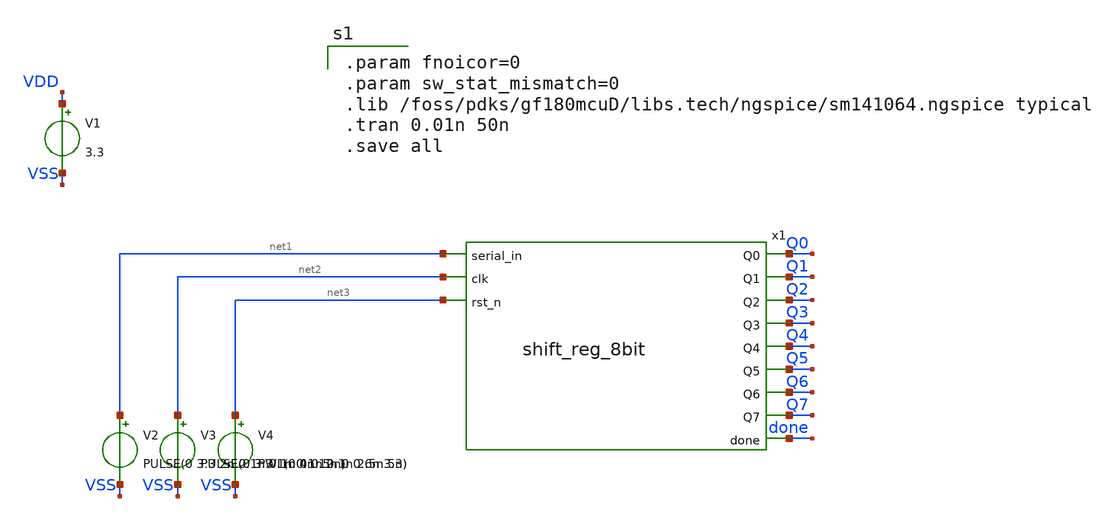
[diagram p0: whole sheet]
** sch_path: xschem/sar_adc/blocks/async_sar/testbench/tb_shift_reg_8bit.sch
**.subckt tb_shift_reg_8bit
V1 VDD VSS 3.3
V2 net1 VSS PULSE(0 3.3 2n 0.1n 0.1n 4n 12n)
V3 net2 VSS PULSE(0 3.3 1n 0.1n 0.1n 2.5n 5n)
V4 net3 VSS PWL(0 0 0.5n 0 0.6n 3.3)
x1 net1 net2 net3 Q0 Q1 Q2 Q3 Q4 Q5 Q6 Q7 done shift_reg_8bit
**** begin user architecture code

.param fnoicor=0
.param sw_stat_mismatch=0
.lib /foss/pdks/gf180mcuD/libs.tech/ngspice/sm141064.ngspice typical
.tran 0.01n 50n
.save all

**** end user architecture code
**.ends

* expanding   symbol:  sar_adc/blocks/async_sar/shift_reg_8bit.sym # of pins=12
** sym_path: xschem/sar_adc/blocks/async_sar/shift_reg_8bit.sym
** sch_path: xschem/sar_adc/blocks/async_sar/shift_reg_8bit.sch
.subckt shift_reg_8bit serial_in clk rst_n Q0 Q1 Q2 Q3 Q4 Q5 Q6 Q7 done
*.ipin serial_in
*.ipin clk
*.ipin rst_n
*.opin Q0
*.opin Q1
*.opin Q2
*.opin Q3
*.opin Q4
*.opin Q5
*.opin Q6
*.opin Q7
*.opin done
x1 Q0 clk rst_n serial_in clk rst_n dff_cell_set
x2 Q0 clk rst_n Q1 dff_cell
x3 Q1 clk rst_n Q2 dff_cell
x4 Q2 clk rst_n Q3 dff_cell
x5 Q3 clk rst_n Q4 dff_cell
x6 Q4 clk rst_n Q5 dff_cell
x7 Q5 clk rst_n Q6 dff_cell
x8 Q6 clk rst_n Q7 dff_cell
x9 Q7 clk rst_n done dff_cell
.ends


* expanding   symbol:  sar_adc/blocks/async_sar/dff_cell_set.sym # of pins=6
** sym_path: xschem/sar_adc/blocks/async_sar/dff_cell_set.sym
** sch_path: xschem/sar_adc/blocks/async_sar/dff_cell_set.sch
.subckt dff_cell_set vdd vss Q D clk rst_n
*.ipin D
*.ipin clk
*.ipin rst_n
*.opin Q
*.iopin vdd
*.iopin vss
x_inv_d vdd D D_b vdd async_inverter
x_dff D_b clk rst_n vdd dff_cell
x_inv_q vdd net1 Q vss async_inverter
.ends


* expanding   symbol:  sar_adc/blocks/async_sar/dff_cell.sym # of pins=4
** sym_path: xschem/sar_adc/dff_cell.sym
** sch_path: xschem/sar_adc/dff_cell.sch
.subckt dff_cell D clk rst_n Q
*.ipin clk
*.ipin D
*.ipin rst_n
*.opin Q
XM1 clk_n clk VDD VDD pfet_03v3 L=0.28u W=1.0u nf=1 ad='int((nf+1)/2) * W/nf * 0.18u' as='int((nf+2)/2) * W/nf * 0.18u'
+ pd='2*int((nf+1)/2) * (W/nf + 0.18u)' ps='2*int((nf+2)/2) * (W/nf + 0.18u)' nrd='0.18u / W' nrs='0.18u / W'
+ sa=0 sb=0 sd=0 m=1
XM2 clk_n clk 0 0 nfet_03v3 L=0.28u W=0.50u nf=1 ad='int((nf+1)/2) * W/nf * 0.18u' as='int((nf+2)/2) * W/nf * 0.18u'
+ pd='2*int((nf+1)/2) * (W/nf + 0.18u)' ps='2*int((nf+2)/2) * (W/nf + 0.18u)' nrd='0.18u / W' nrs='0.18u / W'
+ sa=0 sb=0 sd=0 m=1
XM3 M clk D_int VDD pfet_03v3 L=0.28u W=1.0u nf=1 ad='int((nf+1)/2) * W/nf * 0.18u' as='int((nf+2)/2) * W/nf * 0.18u'
+ pd='2*int((nf+1)/2) * (W/nf + 0.18u)' ps='2*int((nf+2)/2) * (W/nf + 0.18u)' nrd='0.18u / W' nrs='0.18u / W'
+ sa=0 sb=0 sd=0 m=1
XM4 D_int clk_n M 0 nfet_03v3 L=0.28u W=0.50u nf=1 ad='int((nf+1)/2) * W/nf * 0.18u' as='int((nf+2)/2) * W/nf * 0.18u'
+ pd='2*int((nf+1)/2) * (W/nf + 0.18u)' ps='2*int((nf+2)/2) * (W/nf + 0.18u)' nrd='0.18u / W' nrs='0.18u / W'
+ sa=0 sb=0 sd=0 m=1
XM5 M_bar M VDD VDD pfet_03v3 L=0.28u W=1.0u nf=1 ad='int((nf+1)/2) * W/nf * 0.18u' as='int((nf+2)/2) * W/nf * 0.18u'
+ pd='2*int((nf+1)/2) * (W/nf + 0.18u)' ps='2*int((nf+2)/2) * (W/nf + 0.18u)' nrd='0.18u / W' nrs='0.18u / W'
+ sa=0 sb=0 sd=0 m=1
XM6 M_bar M 0 0 nfet_03v3 L=0.28u W=0.50u nf=1 ad='int((nf+1)/2) * W/nf * 0.18u' as='int((nf+2)/2) * W/nf * 0.18u'
+ pd='2*int((nf+1)/2) * (W/nf + 0.18u)' ps='2*int((nf+2)/2) * (W/nf + 0.18u)' nrd='0.18u / W' nrs='0.18u / W'
+ sa=0 sb=0 sd=0 m=1
XM7 M M_bar VDD VDD pfet_03v3 L=2.0u W=0.30u nf=1 ad='int((nf+1)/2) * W/nf * 0.18u' as='int((nf+2)/2) * W/nf * 0.18u'
+ pd='2*int((nf+1)/2) * (W/nf + 0.18u)' ps='2*int((nf+2)/2) * (W/nf + 0.18u)' nrd='0.18u / W' nrs='0.18u / W'
+ sa=0 sb=0 sd=0 m=1
XM8 M M_bar 0 0 nfet_03v3 L=2.4u W=0.22u nf=1 ad='int((nf+1)/2) * W/nf * 0.18u' as='int((nf+2)/2) * W/nf * 0.18u'
+ pd='2*int((nf+1)/2) * (W/nf + 0.18u)' ps='2*int((nf+2)/2) * (W/nf + 0.18u)' nrd='0.18u / W' nrs='0.18u / W'
+ sa=0 sb=0 sd=0 m=1
XM9 S clk_n M_bar VDD pfet_03v3 L=0.28u W=1.0u nf=1 ad='int((nf+1)/2) * W/nf * 0.18u' as='int((nf+2)/2) * W/nf * 0.18u'
+ pd='2*int((nf+1)/2) * (W/nf + 0.18u)' ps='2*int((nf+2)/2) * (W/nf + 0.18u)' nrd='0.18u / W' nrs='0.18u / W'
+ sa=0 sb=0 sd=0 m=1
XM10 M_bar clk S 0 nfet_03v3 L=0.28u W=0.50u nf=1 ad='int((nf+1)/2) * W/nf * 0.18u' as='int((nf+2)/2) * W/nf * 0.18u'
+ pd='2*int((nf+1)/2) * (W/nf + 0.18u)' ps='2*int((nf+2)/2) * (W/nf + 0.18u)' nrd='0.18u / W' nrs='0.18u / W'
+ sa=0 sb=0 sd=0 m=1
XM11 Q_bar S VDD VDD pfet_03v3 L=0.28u W=1.0u nf=1 ad='int((nf+1)/2) * W/nf * 0.18u' as='int((nf+2)/2) * W/nf * 0.18u'
+ pd='2*int((nf+1)/2) * (W/nf + 0.18u)' ps='2*int((nf+2)/2) * (W/nf + 0.18u)' nrd='0.18u / W' nrs='0.18u / W'
+ sa=0 sb=0 sd=0 m=1
XM12 Q_bar rst_n VDD VDD pfet_03v3 L=0.28u W=1.0u nf=1 ad='int((nf+1)/2) * W/nf * 0.18u' as='int((nf+2)/2) * W/nf * 0.18u'
+ pd='2*int((nf+1)/2) * (W/nf + 0.18u)' ps='2*int((nf+2)/2) * (W/nf + 0.18u)' nrd='0.18u / W' nrs='0.18u / W'
+ sa=0 sb=0 sd=0 m=1
XM13 Q_bar S net1 0 nfet_03v3 L=0.28u W=0.50u nf=1 ad='int((nf+1)/2) * W/nf * 0.18u' as='int((nf+2)/2) * W/nf * 0.18u'
+ pd='2*int((nf+1)/2) * (W/nf + 0.18u)' ps='2*int((nf+2)/2) * (W/nf + 0.18u)' nrd='0.18u / W' nrs='0.18u / W'
+ sa=0 sb=0 sd=0 m=1
XM14 net1 rst_n 0 0 nfet_03v3 L=0.28u W=0.50u nf=1 ad='int((nf+1)/2) * W/nf * 0.18u' as='int((nf+2)/2) * W/nf * 0.18u'
+ pd='2*int((nf+1)/2) * (W/nf + 0.18u)' ps='2*int((nf+2)/2) * (W/nf + 0.18u)' nrd='0.18u / W' nrs='0.18u / W'
+ sa=0 sb=0 sd=0 m=1
XM15 Q Q_bar VDD VDD pfet_03v3 L=0.28u W=1.0u nf=1 ad='int((nf+1)/2) * W/nf * 0.18u' as='int((nf+2)/2) * W/nf * 0.18u'
+ pd='2*int((nf+1)/2) * (W/nf + 0.18u)' ps='2*int((nf+2)/2) * (W/nf + 0.18u)' nrd='0.18u / W' nrs='0.18u / W'
+ sa=0 sb=0 sd=0 m=1
XM16 Q Q_bar 0 0 nfet_03v3 L=0.28u W=0.50u nf=1 ad='int((nf+1)/2) * W/nf * 0.18u' as='int((nf+2)/2) * W/nf * 0.18u'
+ pd='2*int((nf+1)/2) * (W/nf + 0.18u)' ps='2*int((nf+2)/2) * (W/nf + 0.18u)' nrd='0.18u / W' nrs='0.18u / W'
+ sa=0 sb=0 sd=0 m=1
XM17 S Q_bar VDD VDD pfet_03v3 L=2.0u W=0.30u nf=1 ad='int((nf+1)/2) * W/nf * 0.18u' as='int((nf+2)/2) * W/nf * 0.18u'
+ pd='2*int((nf+1)/2) * (W/nf + 0.18u)' ps='2*int((nf+2)/2) * (W/nf + 0.18u)' nrd='0.18u / W' nrs='0.18u / W'
+ sa=0 sb=0 sd=0 m=1
XM18 S Q_bar 0 0 nfet_03v3 L=2.4u W=0.22u nf=1 ad='int((nf+1)/2) * W/nf * 0.18u' as='int((nf+2)/2) * W/nf * 0.18u'
+ pd='2*int((nf+1)/2) * (W/nf + 0.18u)' ps='2*int((nf+2)/2) * (W/nf + 0.18u)' nrd='0.18u / W' nrs='0.18u / W'
+ sa=0 sb=0 sd=0 m=1
XM19 D_int D VDD VDD pfet_03v3 L=0.28u W=1.0u nf=1 ad='int((nf+1)/2) * W/nf * 0.18u' as='int((nf+2)/2) * W/nf * 0.18u'
+ pd='2*int((nf+1)/2) * (W/nf + 0.18u)' ps='2*int((nf+2)/2) * (W/nf + 0.18u)' nrd='0.18u / W' nrs='0.18u / W'
+ sa=0 sb=0 sd=0 m=1
XM20 D_int D 0 0 nfet_03v3 L=0.28u W=0.50u nf=1 ad='int((nf+1)/2) * W/nf * 0.18u' as='int((nf+2)/2) * W/nf * 0.18u'
+ pd='2*int((nf+1)/2) * (W/nf + 0.18u)' ps='2*int((nf+2)/2) * (W/nf + 0.18u)' nrd='0.18u / W' nrs='0.18u / W'
+ sa=0 sb=0 sd=0 m=1
.ends


* expanding   symbol:  sar_adc/blocks/async_sar/async_inverter.sym # of pins=4
** sym_path: xschem/sar_adc/blocks/async_sar/async_inverter.sym
** sch_path: xschem/sar_adc/blocks/async_sar/async_inverter.sch
.subckt async_inverter vdd input out vss
*.ipin input
*.opin out
*.iopin vdd
*.iopin vss
XM5 out input vdd vdd pfet_03v3 L=0.28u W=1.00u nf=1 ad='int((nf+1)/2) * W/nf * 0.18u' as='int((nf+2)/2) * W/nf * 0.18u'
+ pd='2*int((nf+1)/2) * (W/nf + 0.18u)' ps='2*int((nf+2)/2) * (W/nf + 0.18u)' nrd='0.18u / W' nrs='0.18u / W'
+ sa=0 sb=0 sd=0 m=1
XM6 out input vss vss nfet_03v3 L=0.28u W=0.50u nf=1 ad='int((nf+1)/2) * W/nf * 0.18u' as='int((nf+2)/2) * W/nf * 0.18u'
+ pd='2*int((nf+1)/2) * (W/nf + 0.18u)' ps='2*int((nf+2)/2) * (W/nf + 0.18u)' nrd='0.18u / W' nrs='0.18u / W'
+ sa=0 sb=0 sd=0 m=1
.ends

.GLOBAL VDD
.end
